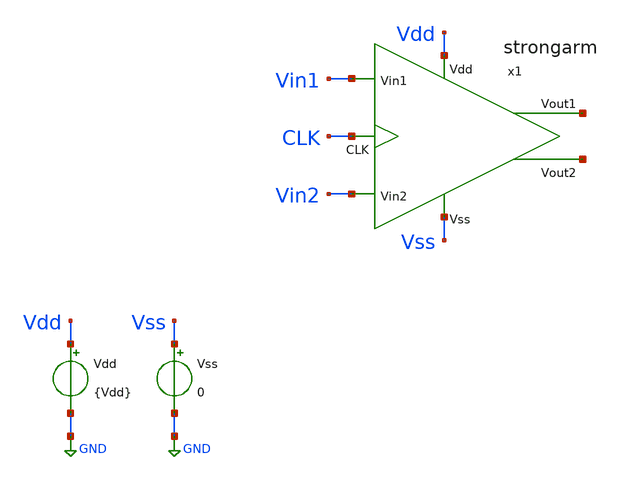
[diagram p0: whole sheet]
** sch_path: xschem/TB/TB_strongarm.sch
**.subckt TB_strongarm
Vdd Vdd GND {Vdd}
x1 net1 net2 Vdd Vss Vin2 Vin1 CLK strongarm
Vss Vss GND 0
**** begin user architecture code


.param Vdd = 1.2
Clk CLK 0 PULSE(0 {Vdd} )



blabla


blabla






**** end user architecture code
**.ends

* expanding   symbol:  ../sch/strongarm.sym # of pins=7
** sym_path: xschem/sch/strongarm.sym
** sch_path: xschem/sch/strongarm.sch
.subckt strongarm Vout2 Vout1 Vdd Vss Vin2 Vin1 CLK
*.ipin Vdd
*.ipin Vss
*.opin Vout2
*.opin Vout1
*.ipin Vin1
*.ipin Vin2
*.ipin Vss
*.ipin Vss
*.ipin CLK
*.ipin CLK
*.ipin CLK
*.ipin Vdd
*.ipin CLK
*.ipin CLK
XM1 net1 Vin1 P Vss sg13_lv_nmos w=1.0u l=0.45u ng=1 m=1 mm_ok=1
XM2 net1 Vin2 Q Vss sg13_lv_nmos w=1.0u l=0.45u ng=1 m=1 mm_ok=1
XM3 P Vout2 Vout1 Vss sg13_lv_nmos w={W34} l={L34} ng=1 m={M34} mm_ok=1
XM4 Q Vout1 Vout2 Vss sg13_lv_nmos w={W34} l={L34} ng=1 m={M34} mm_ok=1
XM6 Vout2 Vout1 Vdd Vdd sg13_lv_pmos w=1.0u l=0.45u ng=1 m=1 mm_ok=1
XM5 Vout1 Vout2 Vdd Vdd sg13_lv_pmos w={W56} l={L56} ng=1 m={M56} mm_ok=1
XM7 Vss CLK net1 Vss sg13_lv_nmos w={W7} l={L7} ng=1 m={M7} mm_ok=1
XM8 P CLK Vdd Vdd sg13_lv_pmos w={W89} l={L89} ng=1 m={M89} mm_ok=1
XM9 Q CLK Vdd Vdd sg13_lv_pmos w=1.0u l=0.45u ng=1 m=1 mm_ok=1
XM11 Vout2 CLK Vdd Vdd sg13_lv_pmos w={Wab} l={Lab} ng=1 m={Wab} mm_ok=1
XM10 Vout1 CLK Vdd Vdd sg13_lv_pmos w={Wab} l={Lab} ng=1 m={Wab} mm_ok=1
.ends

.GLOBAL GND
.end
